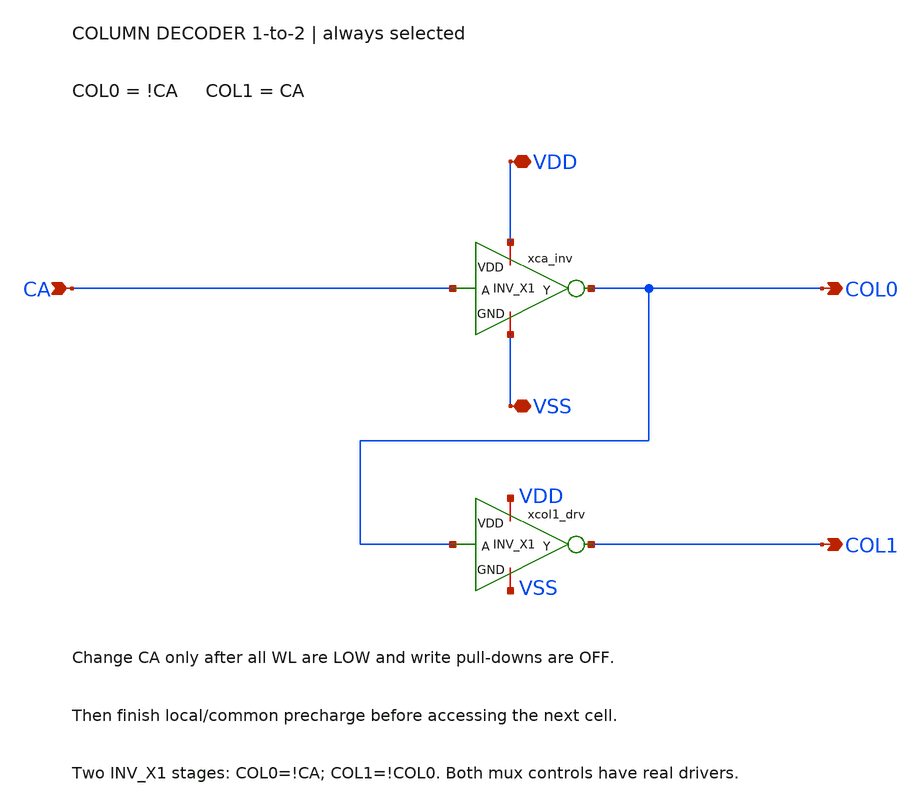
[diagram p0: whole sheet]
** sch_path: member_project/SRAM/PenguinEino/learning/schematics/col_decoder_1to2.sch
**.subckt col_decoder_1to2 CA COL0 COL1 VDD VSS
*.ipin CA
*.opin COL0
*.opin COL1
*.iopin VDD
*.iopin VSS
xca_inv VDD CA COL0 VSS INV_X1
xcol1_drv VDD COL0 COL1 VSS INV_X1
**.ends

* expanding   symbol:  TR-1um_5_stdcell/INV_X1.sym # of pins=4
** sym_path: TR-1um_5_stdcell/INV_X1.sym
** sch_path: TR-1um_5_stdcell/INV_X1.sch
.subckt INV_X1 VDD A Y GND
*.ipin A
*.opin Y
*.iopin GND
*.iopin VDD
XM7 Y A VDD VDD PMOS w=10.2u l=1u as=0 ad=0 ps=0 pd=0 nrd=0 nrs=0 m=1
XM2 Y A GND GND NMOS w=3.4u l=1u as=0 ad=0 ps=0 pd=0 nrd=0 nrs=0 m=1
.ends

.end
